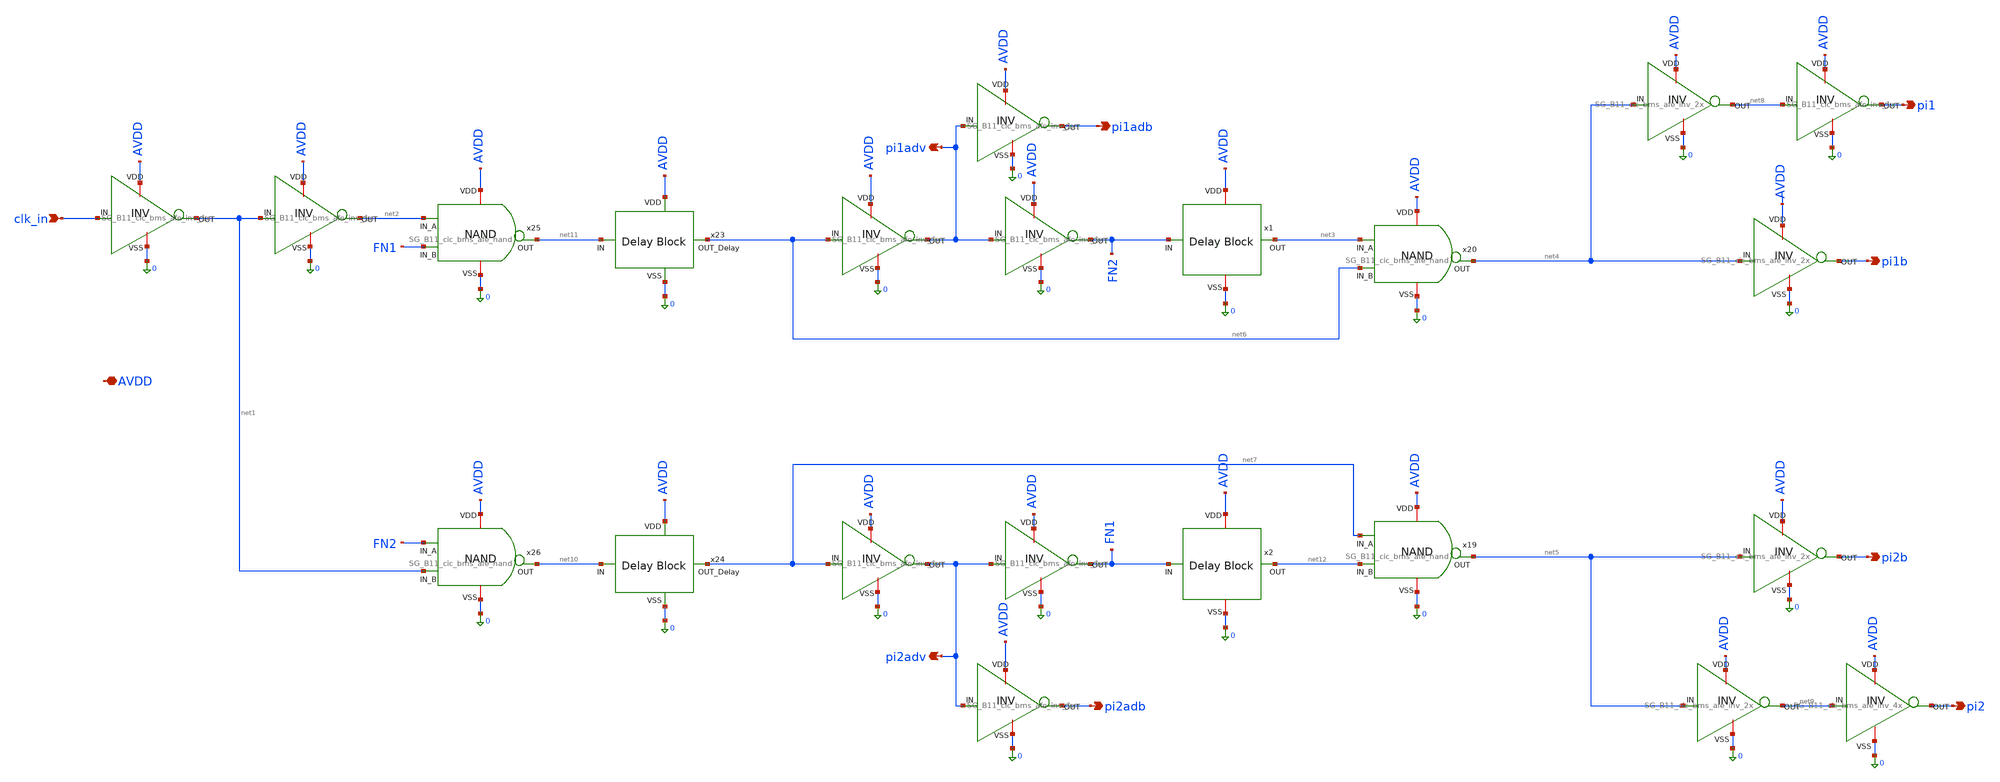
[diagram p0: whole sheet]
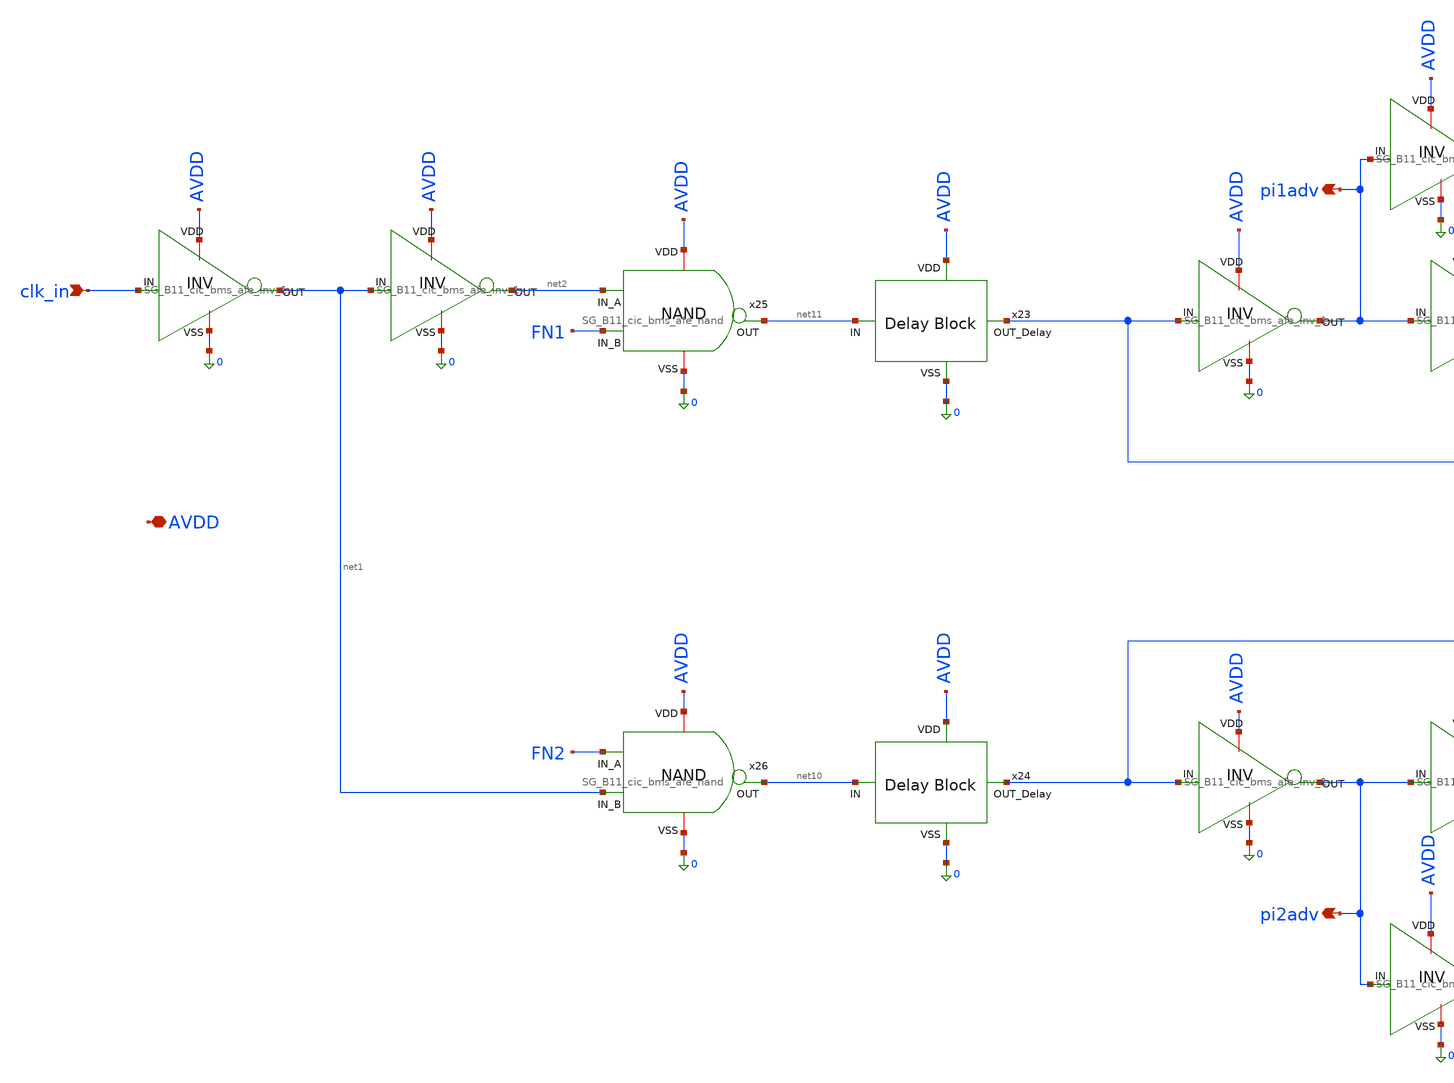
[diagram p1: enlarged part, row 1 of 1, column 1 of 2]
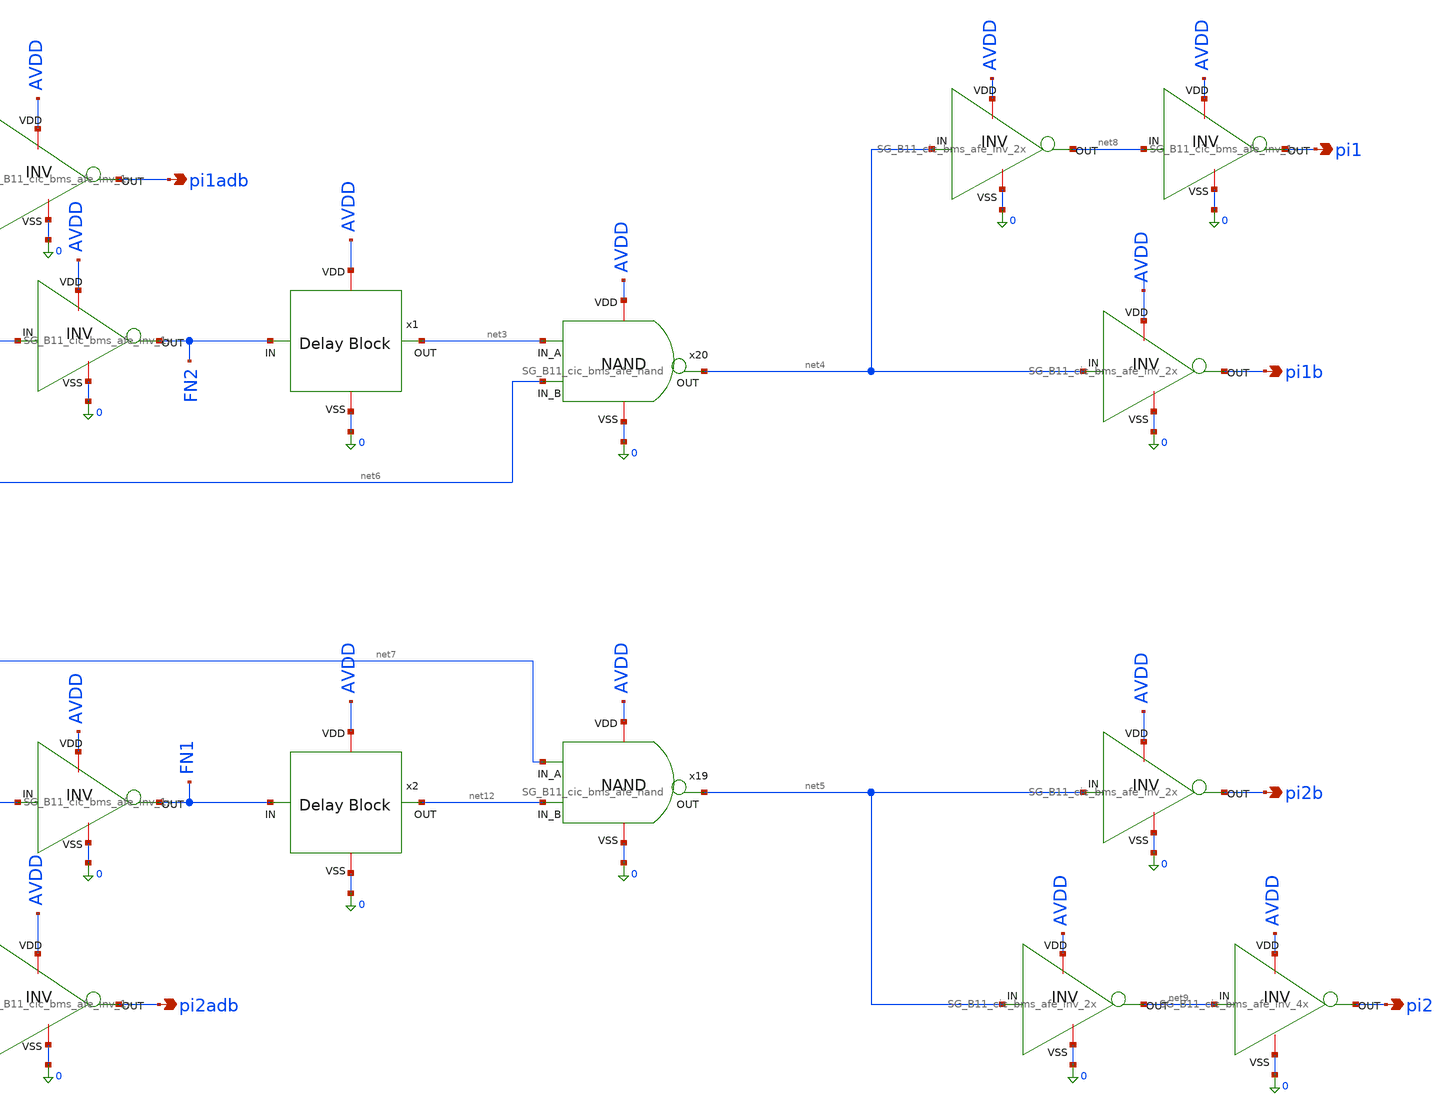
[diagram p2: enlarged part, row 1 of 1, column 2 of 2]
** sch_path: design/schematics/ADC/Non_Overlapping_clk_gen/SG_B11_cic_bms_afe_non_overlapping_clk.sch
**.subckt SG_B11_cic_bms_afe_non_overlapping_clk pi1b pi2b clk_in pi1adb pi2adb pi1adv pi2adv pi1
*+ pi2 AVDD
*.opin pi1b
*.opin pi2b
*.ipin clk_in
*.opin pi1adb
*.opin pi2adb
*.opin pi1adv
*.opin pi2adv
*.opin pi1
*.opin pi2
*.iopin AVDD
x23 AVDD net6 net11 0 SG_B11_cic_bms_afe_delay_block_5V
x24 AVDD net7 net10 0 SG_B11_cic_bms_afe_delay_block_5V
x19 AVDD net12 net7 net5 0 SG_B11_cic_bms_afe_nand
x20 AVDD net6 net3 net4 0 SG_B11_cic_bms_afe_nand
x25 AVDD FN1 net2 net11 0 SG_B11_cic_bms_afe_nand
x26 AVDD net1 FN2 net10 0 SG_B11_cic_bms_afe_nand
x8 AVDD pi1adv net6 0 SG_B11_cic_bms_afe_inv_1x
x11 AVDD pi1adb pi1adv 0 SG_B11_cic_bms_afe_inv_1x
x27 AVDD FN2 pi1adv 0 SG_B11_cic_bms_afe_inv_1x
x28 AVDD FN1 pi2adv 0 SG_B11_cic_bms_afe_inv_1x
x29 AVDD pi2adb pi2adv 0 SG_B11_cic_bms_afe_inv_1x
x30 AVDD pi2adv net7 0 SG_B11_cic_bms_afe_inv_1x
x1 AVDD FN2 net3 0 SG_B11_cic_bms_afe_delay_block_3n
x2 AVDD FN1 net12 0 SG_B11_cic_bms_afe_delay_block_3n
x4 AVDD pi1 net8 0 SG_B11_cic_bms_afe_inv_1x
x5 AVDD net4 net8 0 SG_B11_cic_bms_afe_inv_2x
x9 AVDD net4 pi1b 0 SG_B11_cic_bms_afe_inv_2x
x10 AVDD net5 pi2b 0 SG_B11_cic_bms_afe_inv_2x
x13 AVDD net5 net9 0 SG_B11_cic_bms_afe_inv_2x
x14 AVDD net9 pi2 0 SG_B11_cic_bms_afe_inv_4x
x3 AVDD net1 clk_in 0 SG_B11_cic_bms_afe_inv_1x
x6 AVDD net2 net1 0 SG_B11_cic_bms_afe_inv_1x
**.ends
.end
